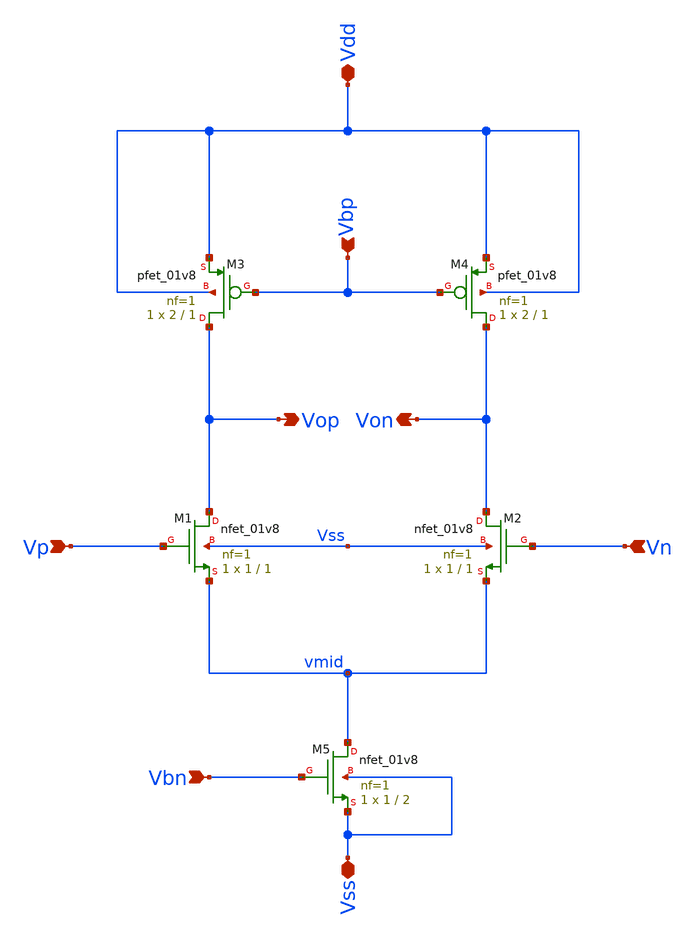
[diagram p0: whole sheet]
** sch_path: Circuits/Examples/OpAmp/DiffAmp.sch
**.subckt DiffAmp Vdd Vss Vp Vn Vbn Vbp Vop Von
*.iopin Vdd
*.iopin Vss
*.ipin Vp
*.ipin Vn
*.ipin Vbn
*.ipin Vbp
*.opin Vop
*.opin Von
XM1 Vop Vp vmid Vss sky130_fd_pr__nfet_01v8 L=1 W=1 nf=1 ad='int((nf+1)/2) * W/nf * 0.29' as='int((nf+2)/2) * W/nf * 0.29'
+ pd='2*int((nf+1)/2) * (W/nf + 0.29)' ps='2*int((nf+2)/2) * (W/nf + 0.29)' nrd='0.29 / W' nrs='0.29 / W'
+ sa=0 sb=0 sd=0 mult=1 m=1
XM2 Von Vn vmid Vss sky130_fd_pr__nfet_01v8 L=1 W=1 nf=1 ad='int((nf+1)/2) * W/nf * 0.29' as='int((nf+2)/2) * W/nf * 0.29'
+ pd='2*int((nf+1)/2) * (W/nf + 0.29)' ps='2*int((nf+2)/2) * (W/nf + 0.29)' nrd='0.29 / W' nrs='0.29 / W'
+ sa=0 sb=0 sd=0 mult=1 m=1
XM3 Vop Vbp Vdd Vdd sky130_fd_pr__pfet_01v8 L=1 W=2 nf=1 ad='int((nf+1)/2) * W/nf * 0.29' as='int((nf+2)/2) * W/nf * 0.29'
+ pd='2*int((nf+1)/2) * (W/nf + 0.29)' ps='2*int((nf+2)/2) * (W/nf + 0.29)' nrd='0.29 / W' nrs='0.29 / W'
+ sa=0 sb=0 sd=0 mult=1 m=1
XM4 Von Vbp Vdd Vdd sky130_fd_pr__pfet_01v8 L=1 W=2 nf=1 ad='int((nf+1)/2) * W/nf * 0.29' as='int((nf+2)/2) * W/nf * 0.29'
+ pd='2*int((nf+1)/2) * (W/nf + 0.29)' ps='2*int((nf+2)/2) * (W/nf + 0.29)' nrd='0.29 / W' nrs='0.29 / W'
+ sa=0 sb=0 sd=0 mult=1 m=1
XM5 vmid Vbn Vss Vss sky130_fd_pr__nfet_01v8 L=2 W=1 nf=1 ad='int((nf+1)/2) * W/nf * 0.29' as='int((nf+2)/2) * W/nf * 0.29'
+ pd='2*int((nf+1)/2) * (W/nf + 0.29)' ps='2*int((nf+2)/2) * (W/nf + 0.29)' nrd='0.29 / W' nrs='0.29 / W'
+ sa=0 sb=0 sd=0 mult=1 m=1
**.ends
.end
